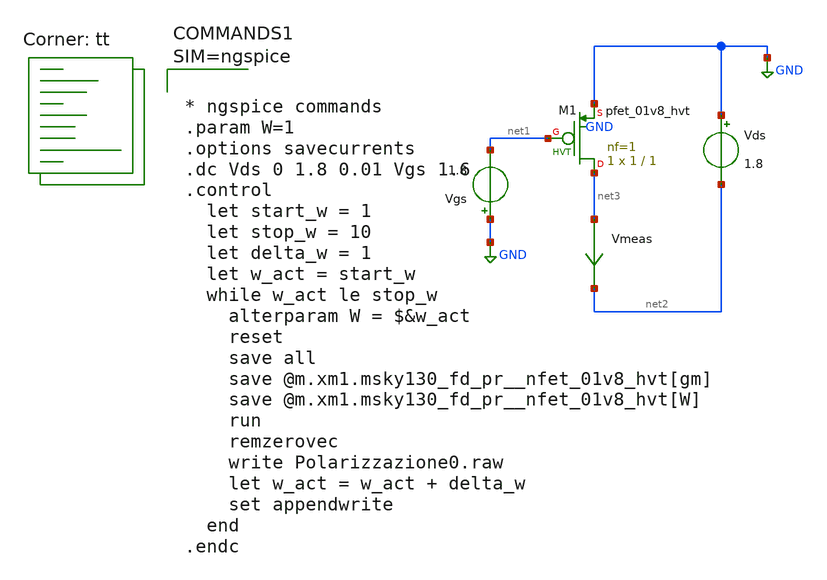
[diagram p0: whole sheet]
** sch_path: xschem/Polarizzazione0.sch
**.subckt Polarizzazione0
Vgs GND net1 1.8
Vds GND net2 1.8
XM1 net3 net1 GND GND sky130_fd_pr__pfet_01v8_hvt L=1 W=1 nf=1 ad='int((nf+1)/2) * W/nf * 0.29' as='int((nf+2)/2) * W/nf * 0.29'
+ pd='2*int((nf+1)/2) * (W/nf + 0.29)' ps='2*int((nf+2)/2) * (W/nf + 0.29)' nrd='0.29 / W' nrs='0.29 / W'
+ sa=0 sb=0 sd=0 mult=1 m=1
Vmeas net3 net2 0
.save i(vmeas)
**** begin user architecture code
.lib $::SKYWATER_MODELS/sky130.lib.spice tt



* ngspice commands
.param W=1
.options savecurrents
.dc Vds 0 1.8 0.01 Vgs 1.6
.control
  let start_w = 1
  let stop_w = 10
  let delta_w = 1
  let w_act = start_w
  while w_act le stop_w
    alterparam W = $&w_act
    reset
    save all
    save @m.xm1.msky130_fd_pr__nfet_01v8_hvt[gm]
    save @m.xm1.msky130_fd_pr__nfet_01v8_hvt[W]
    run
    remzerovec
    write Polarizzazione0.raw
    let w_act = w_act + delta_w
    set appendwrite
  end
.endc



**** end user architecture code
**.ends
.GLOBAL GND
.end
